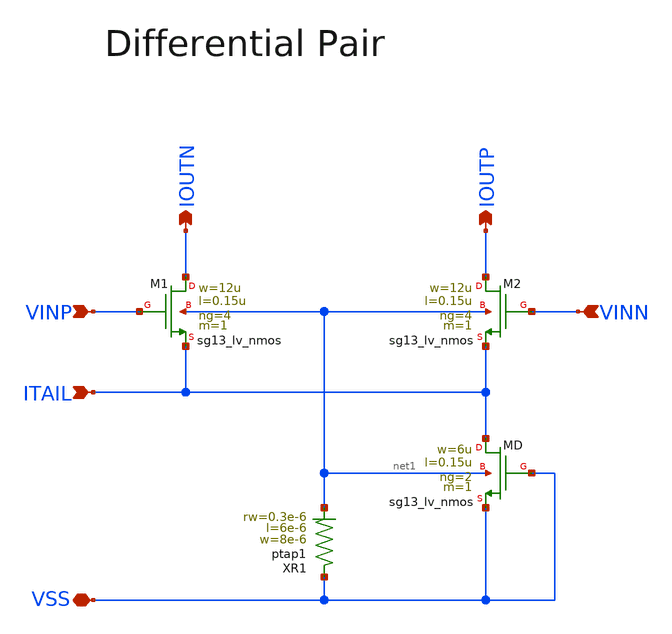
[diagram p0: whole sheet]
** sch_path: dcic_script_differential_pair.sch
* (c) 2026 Julian Schwarz, Apache-2.0 license
**.subckt dcic_script_differential_pair VINP VINN IOUTP IOUTN ITAIL VSS
*.ipin VINP
*.ipin VINN
*.opin IOUTP
*.opin IOUTN
*.ipin ITAIL
*.iopin VSS
XM1 IOUTN VINP ITAIL net1 sg13_lv_nmos w=12u l=0.15u ng=4 m=1 mm_ok=1
XM2 IOUTP VINN ITAIL net1 sg13_lv_nmos w=12u l=0.15u ng=4 m=1 mm_ok=1
XMD ITAIL VSS VSS net1 sg13_lv_nmos w=6u l=0.15u ng=2 m=1 mm_ok=1
XR1 VSS net1 ptap1 R=8.504 w=8e-6 l=6e-6 rw=0.3e-6
**.ends
.end
